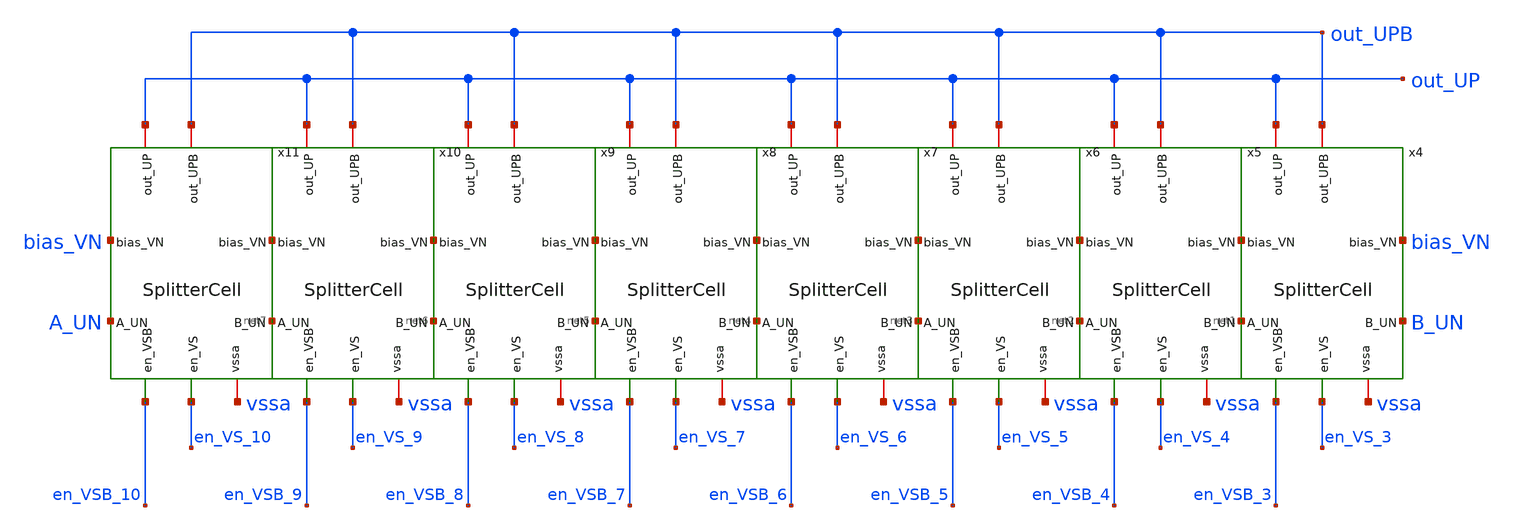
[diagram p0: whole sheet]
** sch_path: lvs/SplitterCells.sch
**.subckt SplitterCells
x4 en_VS_3 net1 B_UN en_VSB_3 bias_VN vssa out_UPB out_UP SplitterCell
x5 en_VS_4 net2 net1 en_VSB_4 bias_VN vssa out_UPB out_UP SplitterCell
x6 en_VS_5 net3 net2 en_VSB_5 bias_VN vssa out_UPB out_UP SplitterCell
x7 en_VS_6 net4 net3 en_VSB_6 bias_VN vssa out_UPB out_UP SplitterCell
x8 en_VS_7 net5 net4 en_VSB_7 bias_VN vssa out_UPB out_UP SplitterCell
x9 en_VS_8 net6 net5 en_VSB_8 bias_VN vssa out_UPB out_UP SplitterCell
x10 en_VS_9 net7 net6 en_VSB_9 bias_VN vssa out_UPB out_UP SplitterCell
x11 en_VS_10 A_UN net7 en_VSB_10 bias_VN vssa out_UPB out_UP SplitterCell
**.ends

* expanding   symbol:  SplitterCell.sym # of pins=9
** sym_path: lvs/SplitterCell.sym
** sch_path: lvs/SplitterCell.sch
.subckt SplitterCell en_VS A_UN B_UN en_VSB bias_VN vssa out_UPB out_UP
*.ipin en_VS
*.ipin en_VSB
*.ipin bias_VN
*.iopin B_UN
*.iopin out_UP
*.iopin out_UPB
*.iopin vssa
*.iopin A_UN
XM_en out_UP en_VS net1 vssa sg13_hv_nmos w=1u l=1u ng=1 m=1 mm_ok=1
XM_enb out_UPB en_VSB net1 vssa sg13_hv_nmos w=1u l=1u ng=1 m=1 mm_ok=1
XM_s1 net1 bias_VN net3 vssa sg13_hv_nmos w=2u l=10u ng=1 m=1 mm_ok=1
XM_s2 net3 bias_VN net4 vssa sg13_hv_nmos w=2u l=10u ng=1 m=1 mm_ok=1
XM_s3 net4 bias_VN net5 vssa sg13_hv_nmos w=2u l=10u ng=1 m=1 mm_ok=1
XM_s4 net5 bias_VN net2 vssa sg13_hv_nmos w=2u l=10u ng=1 m=1 mm_ok=1
XM_s5 net2 bias_VN net6 vssa sg13_hv_nmos w=2u l=10u ng=1 m=1 mm_ok=1
XM_s6 net6 bias_VN net7 vssa sg13_hv_nmos w=2u l=10u ng=1 m=1 mm_ok=1
XM_s7 net7 bias_VN net8 vssa sg13_hv_nmos w=2u l=10u ng=1 m=1 mm_ok=1
XM_s8 net8 bias_VN A_UN vssa sg13_hv_nmos w=2u l=10u ng=1 m=1 mm_ok=1
XM_s9 A_UN bias_VN net9 vssa sg13_hv_nmos w=2u l=10u ng=1 m=1 mm_ok=1
XM_s10 net9 bias_VN net10 vssa sg13_hv_nmos w=2u l=10u ng=1 m=1 mm_ok=1
XM_s11 net10 bias_VN net11 vssa sg13_hv_nmos w=2u l=10u ng=1 m=1 mm_ok=1
XM_s12 net11 bias_VN B_UN vssa sg13_hv_nmos w=2u l=10u ng=1 m=1 mm_ok=1
.ends

.end
